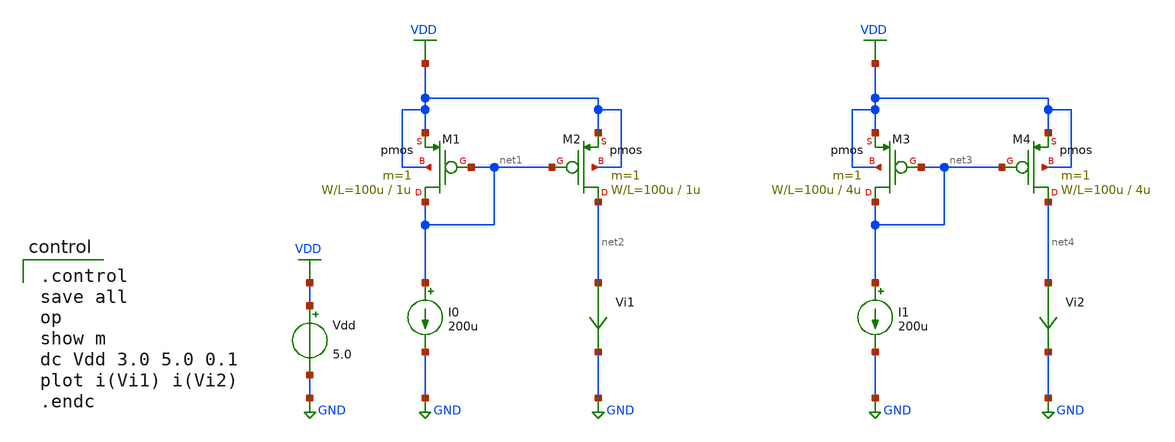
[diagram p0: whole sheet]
** sch_path: OR1/PTC06/opamp/short_channel.sch
**.subckt short_channel
M1 net1 net1 VDD VDD pmos L=1u W=100u m=1
M2 net2 net1 VDD VDD pmos L=1u W=100u m=1
I0 net1 GND 200u
Vi1 net2 GND 0
.save i(vi1)
Vdd VDD GND 5.0
M3 net3 net3 VDD VDD pmos L=4u W=100u m=1
M4 net4 net3 VDD VDD pmos L=4u W=100u m=1
I1 net3 GND 200u
Vi2 net4 GND 0
.save i(vi2)
**** begin user architecture code
 .include $::LIB/mos.lib
.include $::LIB/passive.lib
.include $::LIB/diode.lib

.control
save all
op
show m
dc Vdd 3.0 5.0 0.1
plot i(Vi1) i(Vi2)
.endc

**** end user architecture code
**.ends
.GLOBAL GND
.GLOBAL VDD
.end
